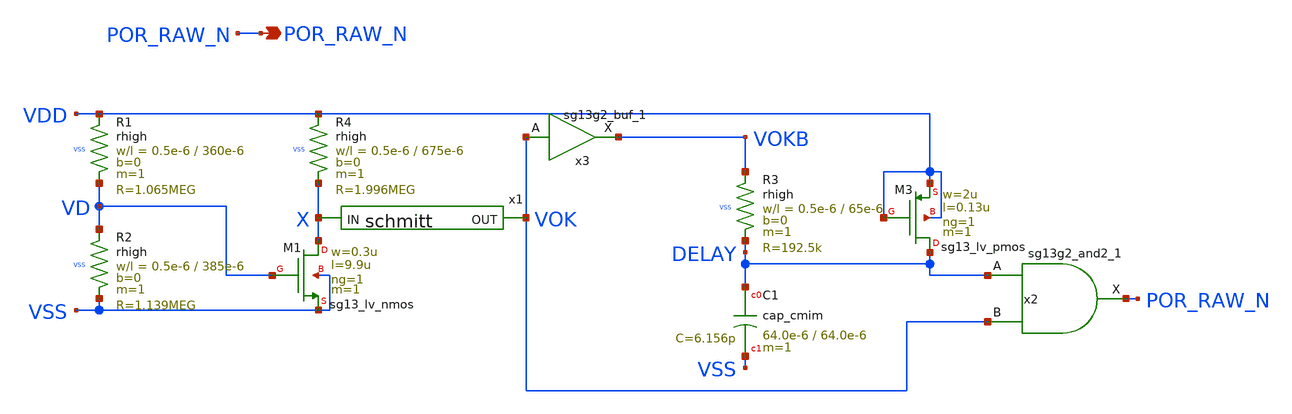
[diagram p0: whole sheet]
** sch_path: design/blocks/por/schematic/wd_por.sch
* IHP-GmbH/IHP-Open-PDK/ihp-sg13g2/libs.tech/xschem/sg13g2_stdcells/sg13g2_buf_1.sch:
* Copyright 2023 IHP PDK Authors
* Licensed under the Apache License, Version 2.0 (the "License");
**.subckt wd_por POR_RAW_N
*.opin POR_RAW_N
XR1 VDD VD VSS rhigh w=0.5e-6 l=360e-6 m=1 b=0 mm_ok=1
XR2 VD VSS VSS rhigh w=0.5e-6 l=385e-6 m=1 b=0 mm_ok=1
XM1 X VD VSS VSS sg13_lv_nmos w=0.3u l=9.9u ng=1 m=1 mm_ok=1
XR3 VOKB DELAY VSS rhigh w=0.5e-6 l=65e-6 m=1 b=0 mm_ok=1
XC1 DELAY VSS cap_cmim w=64.0e-6 l=64.0e-6 m=1 mm_ok=1
XM3 DELAY VDD VDD VDD sg13_lv_pmos w=2u l=0.13u ng=1 m=1 mm_ok=1
x2 POR_RAW_N DELAY VOK VDD VSS sg13g2_and2_1
XR4 VDD X VSS rhigh w=0.5e-6 l=675e-6 m=1 b=0 mm_ok=1
x1 X VOK VDD VSS schmitt
x3 VOKB VOK VDD VSS sg13g2_buf_1
**.ends

* expanding   symbol:  sg13g2_and2_1.sym # of pins=3
** sym_path: sg13g2_and2_1.sym
** sch_path: sg13g2_and2_1.sch
.subckt sg13g2_and2_1 X A B VDD VSS
*.ipin A
*.ipin B
*.opin X
*.iopin VDD
*.iopin VSS
XM1 net1 A net2 VSS sg13_lv_nmos w=640.00n l=130.00n ng=1 m=1 mm_ok=1
XM2 net2 B VSS VSS sg13_lv_nmos w=640.00n l=130.00n ng=1 m=1 mm_ok=1
XM3 X net1 VSS VSS sg13_lv_nmos w=740.00n l=130.00n ng=1 m=1 mm_ok=1
XM4 net1 B VDD VDD sg13_lv_pmos w=840.00n l=130.00n ng=1 m=1 mm_ok=1
XM5 net1 A VDD VDD sg13_lv_pmos w=840.00n l=130.00n ng=1 m=1 mm_ok=1
XM6 X net1 VDD VDD sg13_lv_pmos w=1.12u l=130.00n ng=1 m=1 mm_ok=1
.ends


* expanding   symbol:  schmitt.sym # of pins=2
** sym_path: design/blocks/schmitt/schematic/schmitt.sym
** sch_path: design/blocks/schmitt/schematic/schmitt.sch
.subckt schmitt IN OUT VDD VSS
*.opin OUT
*.ipin IN
XM4 net1 IN VDD VDD sg13_lv_pmos w=1.04u l=0.13u ng=1 m=1 mm_ok=1
XM6 OUT IN net2 VSS sg13_lv_nmos w=0.76u l=0.13u ng=1 m=1 mm_ok=1
XM5 OUT IN net1 VDD sg13_lv_pmos w=1.04u l=0.13u ng=1 m=1 mm_ok=1
XM7 net2 IN VSS VSS sg13_lv_nmos w=0.76u l=0.13u ng=1 m=1 mm_ok=1
XM8 VSS OUT net1 VDD sg13_lv_pmos w=0.42u l=0.13u ng=1 m=1 mm_ok=1
XM9 VDD OUT net2 VSS sg13_lv_nmos w=0.42u l=0.13u ng=1 m=1 mm_ok=1
.ends


* expanding   symbol:  sg13g2_buf_1.sym # of pins=2
** sym_path: sg13g2_buf_1.sym
** sch_path: sg13g2_buf_1.sch
.subckt sg13g2_buf_1 X A VDD VSS
*.ipin A
*.opin X
*.iopin VDD
*.iopin VSS
XM1 net1 A VSS VSS sg13_lv_nmos w=550.00n l=130.00n ng=1 m=1 mm_ok=1
XM2 X net1 VSS VSS sg13_lv_nmos w=740.00n l=130.00n ng=1 m=1 mm_ok=1
XM3 net1 A VDD VDD sg13_lv_pmos w=840.00n l=130.00n ng=1 m=1 mm_ok=1
XM4 X net1 VDD VDD sg13_lv_pmos w=1.12u l=130.00n ng=1 m=1 mm_ok=1
.ends

.end
